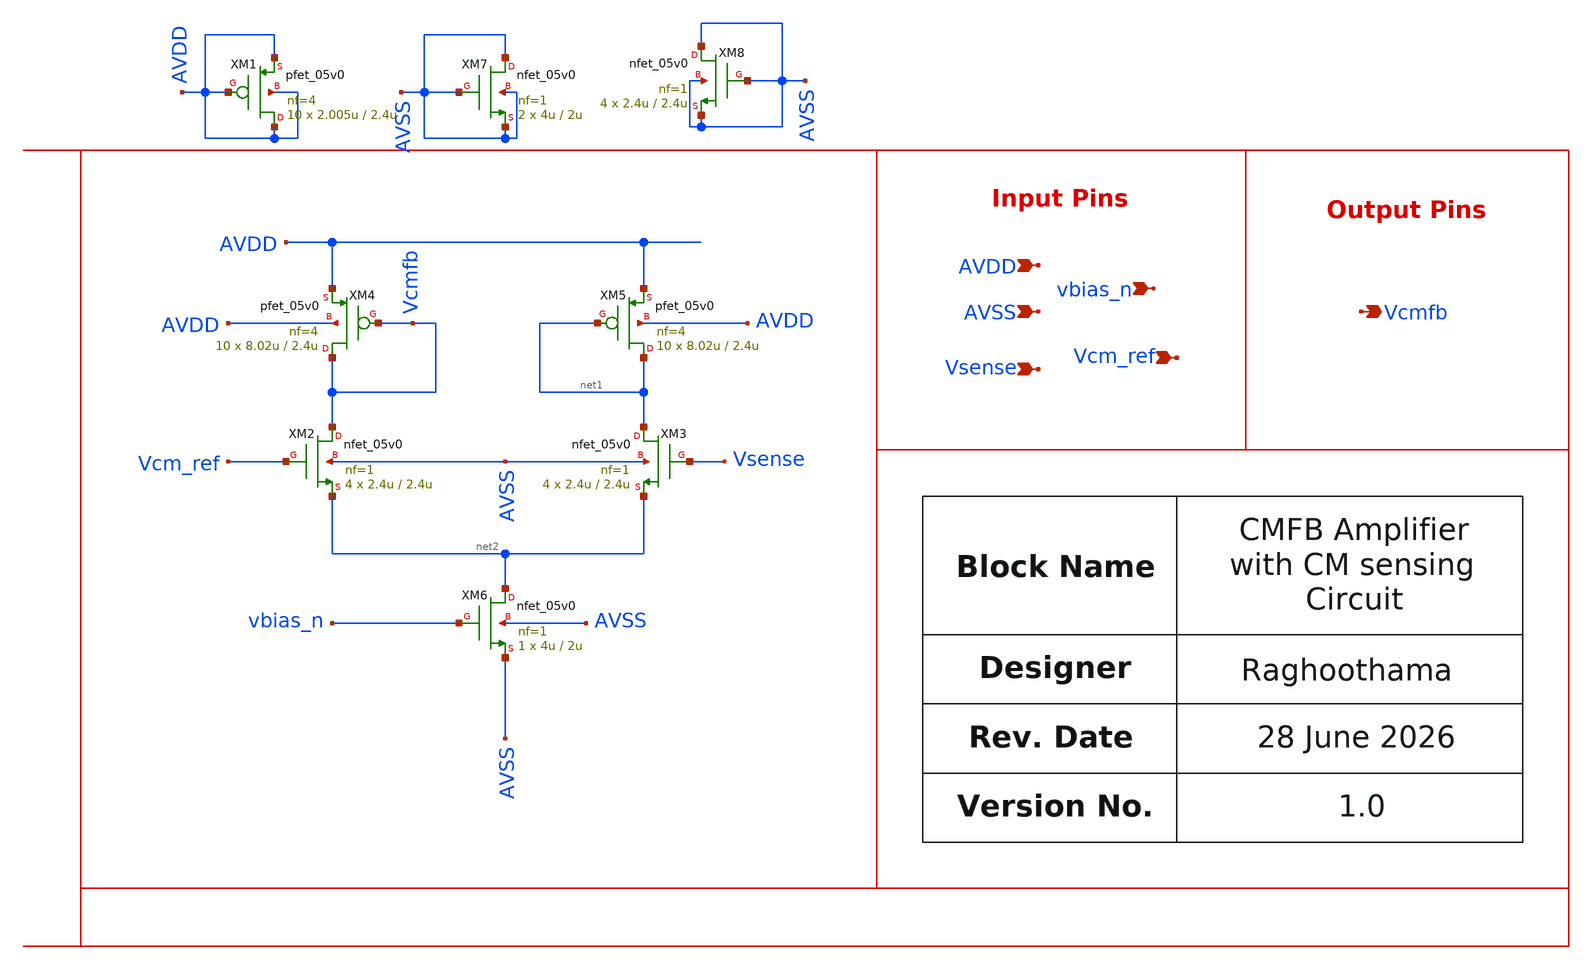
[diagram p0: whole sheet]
** sch_path: design/schematics/ADC/Adder/OTA/rrao_cic_bms_afe_iadc_second_int_ota_cmfb.sch
**.subckt rrao_cic_bms_afe_iadc_second_int_ota_cmfb Vcm_ref Vcmfb AVSS vbias_n AVDD Vsense
*.ipin Vcm_ref
*.opin Vcmfb
*.ipin AVSS
*.ipin vbias_n
*.ipin AVDD
*.ipin Vsense
XM2 Vcmfb Vcm_ref net2 AVSS nfet_05v0 L=2.4u W=2.4u nf=1 ad='int((nf+1)/2) * W/nf * 0.18u' as='int((nf+2)/2) * W/nf * 0.18u'
+ pd='2*int((nf+1)/2) * (W/nf + 0.18u)' ps='2*int((nf+2)/2) * (W/nf + 0.18u)' nrd='0.18u / W' nrs='0.18u / W'
+ sa=0 sb=0 sd=0 m=4
XM3 net1 Vsense net2 AVSS nfet_05v0 L=2.4u W=2.4u nf=1 ad='int((nf+1)/2) * W/nf * 0.18u' as='int((nf+2)/2) * W/nf * 0.18u'
+ pd='2*int((nf+1)/2) * (W/nf + 0.18u)' ps='2*int((nf+2)/2) * (W/nf + 0.18u)' nrd='0.18u / W' nrs='0.18u / W'
+ sa=0 sb=0 sd=0 m=4
XM4 Vcmfb Vcmfb AVDD AVDD pfet_05v0 L=2.4u W=8.02u nf=4 ad='int((nf+1)/2) * W/nf * 0.18u' as='int((nf+2)/2) * W/nf * 0.18u'
+ pd='2*int((nf+1)/2) * (W/nf + 0.18u)' ps='2*int((nf+2)/2) * (W/nf + 0.18u)' nrd='0.18u / W' nrs='0.18u / W'
+ sa=0 sb=0 sd=0 m=10
XM5 net1 net1 AVDD AVDD pfet_05v0 L=2.4u W=8.02u nf=4 ad='int((nf+1)/2) * W/nf * 0.18u' as='int((nf+2)/2) * W/nf * 0.18u'
+ pd='2*int((nf+1)/2) * (W/nf + 0.18u)' ps='2*int((nf+2)/2) * (W/nf + 0.18u)' nrd='0.18u / W' nrs='0.18u / W'
+ sa=0 sb=0 sd=0 m=10
XM6 net2 vbias_n AVSS AVSS nfet_05v0 L=2u W=4u nf=1 ad='int((nf+1)/2) * W/nf * 0.18u' as='int((nf+2)/2) * W/nf * 0.18u'
+ pd='2*int((nf+1)/2) * (W/nf + 0.18u)' ps='2*int((nf+2)/2) * (W/nf + 0.18u)' nrd='0.18u / W' nrs='0.18u / W'
+ sa=0 sb=0 sd=0 m=1
XM1 AVDD AVDD AVDD AVDD pfet_05v0 L=2.4u W=2.005u nf=4 ad='int((nf+1)/2) * W/nf * 0.18u' as='int((nf+2)/2) * W/nf * 0.18u'
+ pd='2*int((nf+1)/2) * (W/nf + 0.18u)' ps='2*int((nf+2)/2) * (W/nf + 0.18u)' nrd='0.18u / W' nrs='0.18u / W'
+ sa=0 sb=0 sd=0 m=10
XM7 AVSS AVSS AVSS AVSS nfet_05v0 L=2u W=4u nf=1 ad='int((nf+1)/2) * W/nf * 0.18u' as='int((nf+2)/2) * W/nf * 0.18u'
+ pd='2*int((nf+1)/2) * (W/nf + 0.18u)' ps='2*int((nf+2)/2) * (W/nf + 0.18u)' nrd='0.18u / W' nrs='0.18u / W'
+ sa=0 sb=0 sd=0 m=2
XM8 AVSS AVSS AVSS AVSS nfet_05v0 L=2.4u W=2.4u nf=1 ad='int((nf+1)/2) * W/nf * 0.18u' as='int((nf+2)/2) * W/nf * 0.18u'
+ pd='2*int((nf+1)/2) * (W/nf + 0.18u)' ps='2*int((nf+2)/2) * (W/nf + 0.18u)' nrd='0.18u / W' nrs='0.18u / W'
+ sa=0 sb=0 sd=0 m=4
**.ends
.end
